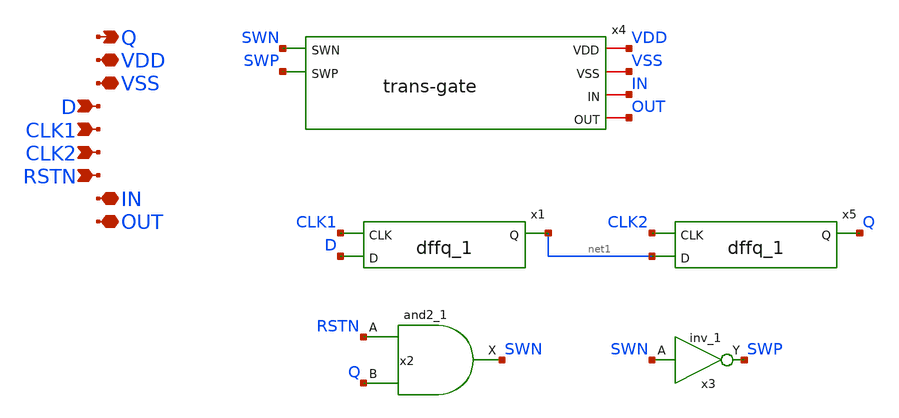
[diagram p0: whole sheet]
** sch_path: designs/libs/core_switch-matrix/switch-cell/switch-cell.sch
**.subckt switch-cell VDD VSS CLK1 D IN OUT RSTN Q CLK2
*.iopin VDD
*.iopin VSS
*.ipin CLK1
*.ipin D
*.iopin IN
*.iopin OUT
*.ipin RSTN
*.opin Q
*.ipin CLK2
x4 VDD VSS SWN SWP IN OUT trans-gate
x1 D CLK1 net1 VDDd VDDd VSSd VSSd gf180mcu_fd_sc_mcu9t5v0__dffq_1
x5 net1 CLK2 Q VDDd VDDd VSSd VSSd gf180mcu_fd_sc_mcu9t5v0__dffq_1
x2 RSTN Q VSSd VDDd VSSd VDDd SWN gf180mcu_fd_sc_mcu9t5v0__and2_1
x3 SWN VSSd VDDd VSSd VDDd SWP gf180mcu_fd_sc_mcu9t5v0__inv_1
**.ends

* expanding   symbol:  core_switch-matrix/trans-gate/trans-gate.sym # of pins=6
** sym_path: designs/libs/core_switch-matrix/trans-gate/trans-gate.sym
** sch_path: designs/libs/core_switch-matrix/trans-gate/trans-gate.sch
.subckt trans-gate VDD VSS SWN SWP IN OUT
*.iopin VDD
*.iopin VSS
*.iopin IN
*.iopin OUT
*.ipin SWN
*.ipin SWP
XM3 IN SWN OUT VSS nfet_03v3 L=0.70u W=8u nf=1 ad='int((nf+1)/2) * W/nf * 0.18u' as='int((nf+2)/2) * W/nf * 0.18u'
+ pd='2*int((nf+1)/2) * (W/nf + 0.18u)' ps='2*int((nf+2)/2) * (W/nf + 0.18u)' nrd='0.18u / W' nrs='0.18u / W'
+ sa=0 sb=0 sd=0 m=3
XM2 IN SWP OUT VDD pfet_03v3 L=0.55u W=8u nf=1 ad='int((nf+1)/2) * W/nf * 0.18u' as='int((nf+2)/2) * W/nf * 0.18u'
+ pd='2*int((nf+1)/2) * (W/nf + 0.18u)' ps='2*int((nf+2)/2) * (W/nf + 0.18u)' nrd='0.18u / W' nrs='0.18u / W'
+ sa=0 sb=0 sd=0 m=9
.ends

.end
